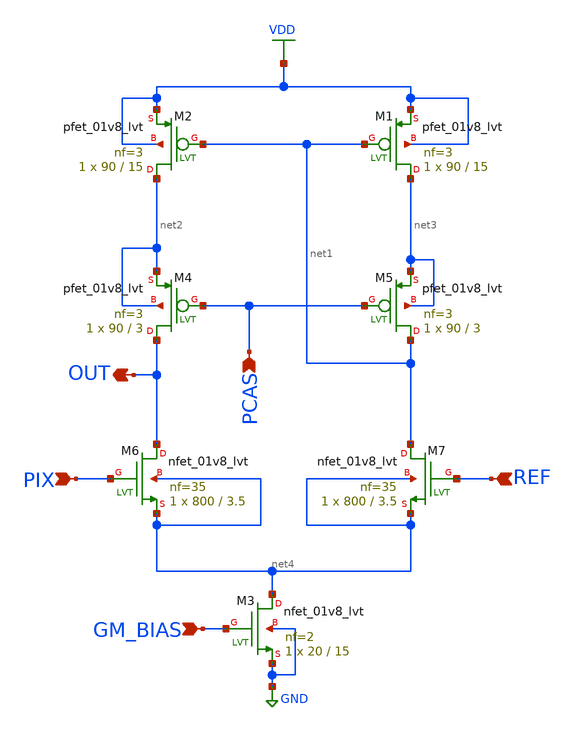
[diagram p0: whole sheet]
** sch_path: xschem/diffamp/diffamp.sch
**.subckt diffamp PCAS PIX REF GM_BIAS OUT
*.ipin PCAS
*.ipin PIX
*.ipin REF
*.ipin GM_BIAS
*.opin OUT
XM4 OUT PCAS net2 net2 sky130_fd_pr__pfet_01v8_lvt L=3 W=90 nf=3 ad='int((3 + 1)/2) * 90 / 3 * 0.29'
+ as='int((3 + 2)/2) * 90 / 3 * 0.29' pd='2*int((3 + 1)/2) * (90 / 3 + 0.29)' ps='2*int((3 + 2)/2) * (90 / 3 + 0.29)'
+ nrd='0.29 / 90 ' nrs='0.29 / 90 ' sa=0 sb=0 sd=0 mult=1 m=1
XM5 net1 PCAS net3 net3 sky130_fd_pr__pfet_01v8_lvt L=3 W=90 nf=3 ad='int((3 + 1)/2) * 90 / 3 * 0.29'
+ as='int((3 + 2)/2) * 90 / 3 * 0.29' pd='2*int((3 + 1)/2) * (90 / 3 + 0.29)' ps='2*int((3 + 2)/2) * (90 / 3 + 0.29)'
+ nrd='0.29 / 90 ' nrs='0.29 / 90 ' sa=0 sb=0 sd=0 mult=1 m=1
XM6 OUT PIX net4 net4 sky130_fd_pr__nfet_01v8_lvt L=3.5 W=800 nf=35 ad='int((35 + 1)/2) * 800 / 35 * 0.29'
+ as='int((35 + 2)/2) * 800 / 35 * 0.29' pd='2*int((35 + 1)/2) * (800 / 35 + 0.29)' ps='2*int((35 + 2)/2) * (800 / 35 + 0.29)'
+ nrd='0.29 / 800 ' nrs='0.29 / 800 ' sa=0 sb=0 sd=0 mult=1 m=1
XM7 net1 REF net4 net4 sky130_fd_pr__nfet_01v8_lvt L=3.5 W=800 nf=35 ad='int((35 + 1)/2) * 800 / 35 * 0.29'
+ as='int((35 + 2)/2) * 800 / 35 * 0.29' pd='2*int((35 + 1)/2) * (800 / 35 + 0.29)' ps='2*int((35 + 2)/2) * (800 / 35 + 0.29)'
+ nrd='0.29 / 800 ' nrs='0.29 / 800 ' sa=0 sb=0 sd=0 mult=1 m=1
XM1 net3 net1 VDD VDD sky130_fd_pr__pfet_01v8_lvt L=15 W=90 nf=3 ad='int((3 + 1)/2) * 90 / 3 * 0.29'
+ as='int((3 + 2)/2) * 90 / 3 * 0.29' pd='2*int((3 + 1)/2) * (90 / 3 + 0.29)' ps='2*int((3 + 2)/2) * (90 / 3 + 0.29)'
+ nrd='0.29 / 90 ' nrs='0.29 / 90 ' sa=0 sb=0 sd=0 mult=1 m=1
XM2 net2 net1 VDD VDD sky130_fd_pr__pfet_01v8_lvt L=15 W=90 nf=3 ad='int((3 + 1)/2) * 90 / 3 * 0.29'
+ as='int((3 + 2)/2) * 90 / 3 * 0.29' pd='2*int((3 + 1)/2) * (90 / 3 + 0.29)' ps='2*int((3 + 2)/2) * (90 / 3 + 0.29)'
+ nrd='0.29 / 90 ' nrs='0.29 / 90 ' sa=0 sb=0 sd=0 mult=1 m=1
XM3 net4 GM_BIAS GND GND sky130_fd_pr__nfet_01v8_lvt L=15 W=20 nf=2 ad='int((2 + 1)/2) * 20 / 2 * 0.29'
+ as='int((2 + 2)/2) * 20 / 2 * 0.29' pd='2*int((2 + 1)/2) * (20 / 2 + 0.29)' ps='2*int((2 + 2)/2) * (20 / 2 + 0.29)'
+ nrd='0.29 / 20 ' nrs='0.29 / 20 ' sa=0 sb=0 sd=0 mult=1 m=1
**.ends
.GLOBAL GND
.GLOBAL VDD
.end
